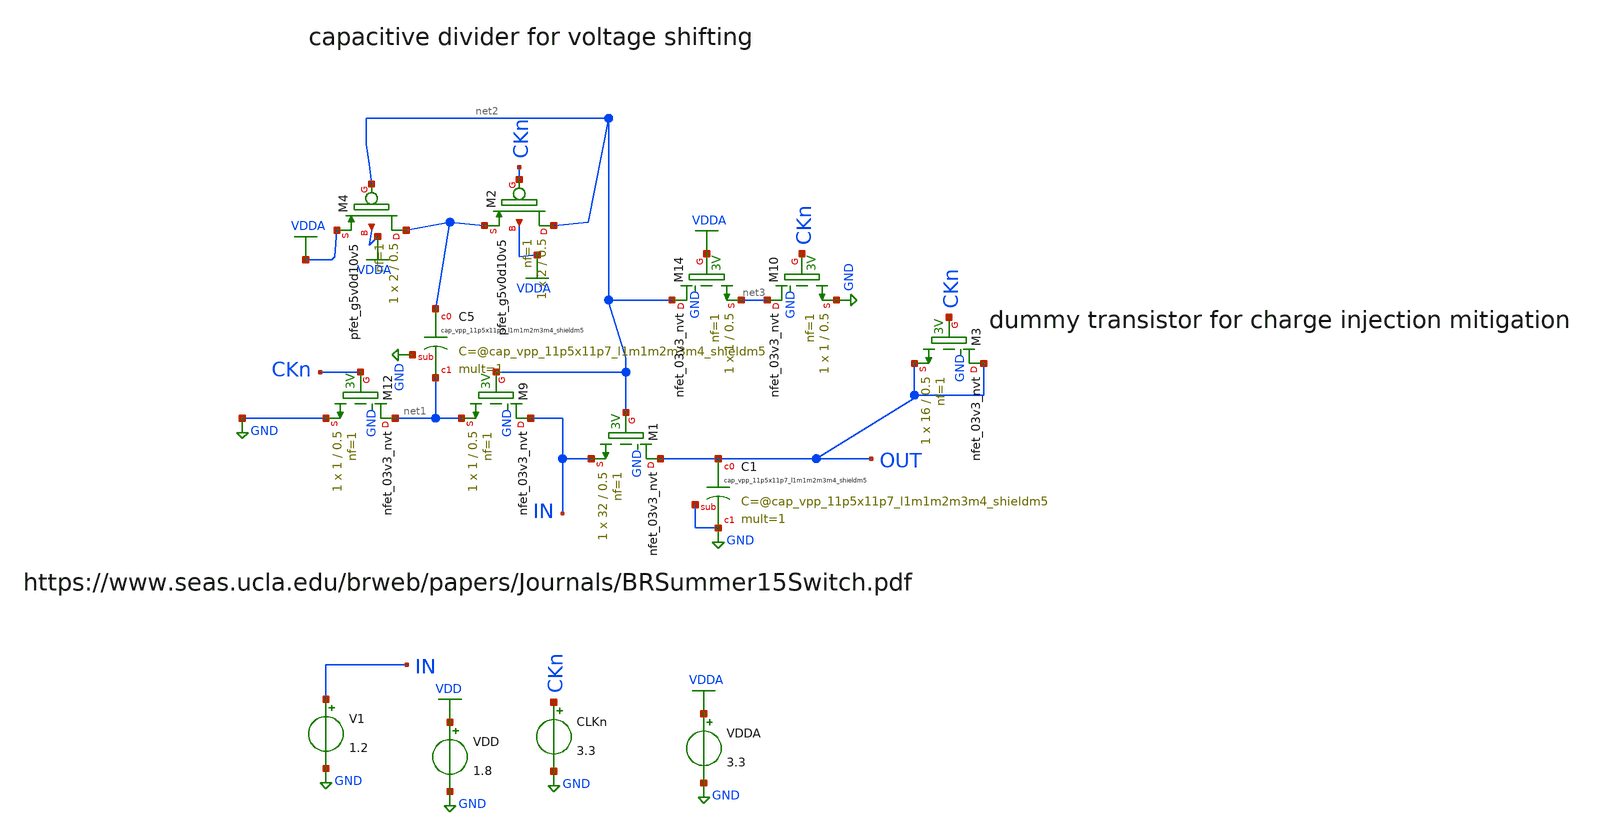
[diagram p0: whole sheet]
** sch_path: xschem/bootstrapped_switch.sch
**.subckt bootstrapped_switch
XM12 net1 CKn GND GND sky130_fd_pr__nfet_03v3_nvt L=0.5 W=1 nf=1 ad='int((1 + 1)/2) * 1 / 1 * 0.29' as='int((1 + 2)/2) * 1 / 1 * 0.29'
+ pd='2*int((1 + 1)/2) * (1 / 1 + 0.29)' ps='2*int((1 + 2)/2) * (1 / 1 + 0.29)' nrd='0.29 / 1 ' nrs='0.29 / 1 '
+ sa=0 sb=0 sd=0 mult=1 m=1
XC5 net4 net1 GND sky130_fd_pr__cap_vpp_11p5x11p7_l1m1m2m3m4_shieldm5 mult=1 m=1
VDD VDD GND 1.8
V1 IN GND 1.2
XM9 IN net2 net1 GND sky130_fd_pr__nfet_03v3_nvt L=0.5 W=1 nf=1 ad='int((1 + 1)/2) * 1 / 1 * 0.29' as='int((1 + 2)/2) * 1 / 1 * 0.29'
+ pd='2*int((1 + 1)/2) * (1 / 1 + 0.29)' ps='2*int((1 + 2)/2) * (1 / 1 + 0.29)' nrd='0.29 / 1 ' nrs='0.29 / 1 '
+ sa=0 sb=0 sd=0 mult=1 m=1
XM1 OUT net2 IN GND sky130_fd_pr__nfet_03v3_nvt L=0.5 W=32 nf=1 ad='int((1 + 1)/2) * 32 / 1 * 0.29' as='int((1 + 2)/2) * 32 / 1 * 0.29'
+ pd='2*int((1 + 1)/2) * (32 / 1 + 0.29)' ps='2*int((1 + 2)/2) * (32 / 1 + 0.29)' nrd='0.29 / 32 ' nrs='0.29 / 32 '
+ sa=0 sb=0 sd=0 mult=1 m=1
XC1 OUT GND GND sky130_fd_pr__cap_vpp_11p5x11p7_l1m1m2m3m4_shieldm5 mult=1 m=1
CLKn CKn GND 3.3
XM14 net2 VDDA net3 GND sky130_fd_pr__nfet_03v3_nvt L=0.5 W=1 nf=1 ad='int((1 + 1)/2) * 1 / 1 * 0.29'
+ as='int((1 + 2)/2) * 1 / 1 * 0.29' pd='2*int((1 + 1)/2) * (1 / 1 + 0.29)' ps='2*int((1 + 2)/2) * (1 / 1 + 0.29)'
+ nrd='0.29 / 1 ' nrs='0.29 / 1 ' sa=0 sb=0 sd=0 mult=1 m=1
XM10 net3 CKn GND GND sky130_fd_pr__nfet_03v3_nvt L=0.5 W=1 nf=1 ad='int((1 + 1)/2) * 1 / 1 * 0.29' as='int((1 + 2)/2) * 1 / 1 * 0.29'
+ pd='2*int((1 + 1)/2) * (1 / 1 + 0.29)' ps='2*int((1 + 2)/2) * (1 / 1 + 0.29)' nrd='0.29 / 1 ' nrs='0.29 / 1 '
+ sa=0 sb=0 sd=0 mult=1 m=1
XM3 OUT CKn OUT GND sky130_fd_pr__nfet_03v3_nvt L=0.5 W=16 nf=1 ad='int((1 + 1)/2) * 16 / 1 * 0.29' as='int((1 + 2)/2) * 16 / 1 * 0.29'
+ pd='2*int((1 + 1)/2) * (16 / 1 + 0.29)' ps='2*int((1 + 2)/2) * (16 / 1 + 0.29)' nrd='0.29 / 16 ' nrs='0.29 / 16 '
+ sa=0 sb=0 sd=0 mult=1 m=1
VDDA VDDA GND 3.3
XM2 net2 CKn net4 VDDA sky130_fd_pr__pfet_g5v0d10v5 L=0.5 W=2 nf=1 ad='int((1 + 1)/2) * 2 / 1 * 0.29'
+ as='int((1 + 2)/2) * 2 / 1 * 0.29' pd='2*int((1 + 1)/2) * (2 / 1 + 0.29)' ps='2*int((1 + 2)/2) * (2 / 1 + 0.29)'
+ nrd='0.29 / 2 ' nrs='0.29 / 2 ' sa=0 sb=0 sd=0 mult=1 m=1
XM4 net4 net2 VDDA VDDA sky130_fd_pr__pfet_g5v0d10v5 L=0.5 W=2 nf=1 ad='int((1 + 1)/2) * 2 / 1 * 0.29'
+ as='int((1 + 2)/2) * 2 / 1 * 0.29' pd='2*int((1 + 1)/2) * (2 / 1 + 0.29)' ps='2*int((1 + 2)/2) * (2 / 1 + 0.29)'
+ nrd='0.29 / 2 ' nrs='0.29 / 2 ' sa=0 sb=0 sd=0 mult=1 m=1
**** begin user architecture code

** opencircuitdesign pdks install
.lib $::SKYWATER_MODELS/sky130.lib.spice tt


**** end user architecture code
**.ends
.GLOBAL GND
.GLOBAL VDD
.GLOBAL VDDA
.end
